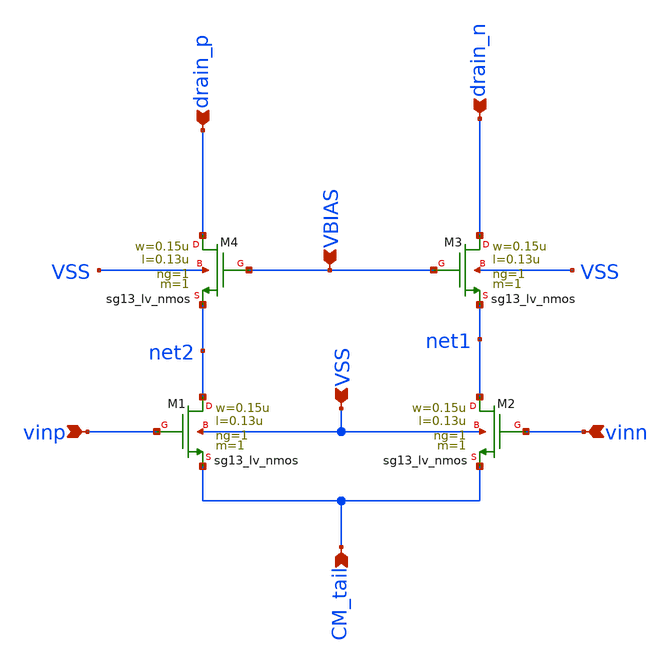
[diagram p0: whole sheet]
** sch_path: analog-db/templates/miscellaneous/diff_pair_improved_nmos.sch
* Copyright 2026 MacAnalog Research Group
**.subckt diff_pair_improved_nmos vinp vinn CM_tail drain_n drain_p VSS VBIAS
*.ipin vinp
*.ipin vinn
*.ipin CM_tail
*.ipin drain_n
*.ipin drain_p
*.ipin VSS
*.ipin VBIAS
XM1 net2 vinp CM_tail VSS sg13_lv_nmos w=0.15u l=0.13u ng=1 m=1 mm_ok=1
XM2 net1 vinn CM_tail VSS sg13_lv_nmos w=0.15u l=0.13u ng=1 m=1 mm_ok=1
XM3 drain_n VBIAS net1 VSS sg13_lv_nmos w=0.15u l=0.13u ng=1 m=1 mm_ok=1
XM4 drain_p VBIAS net2 VSS sg13_lv_nmos w=0.15u l=0.13u ng=1 m=1 mm_ok=1
**.ends
.end
